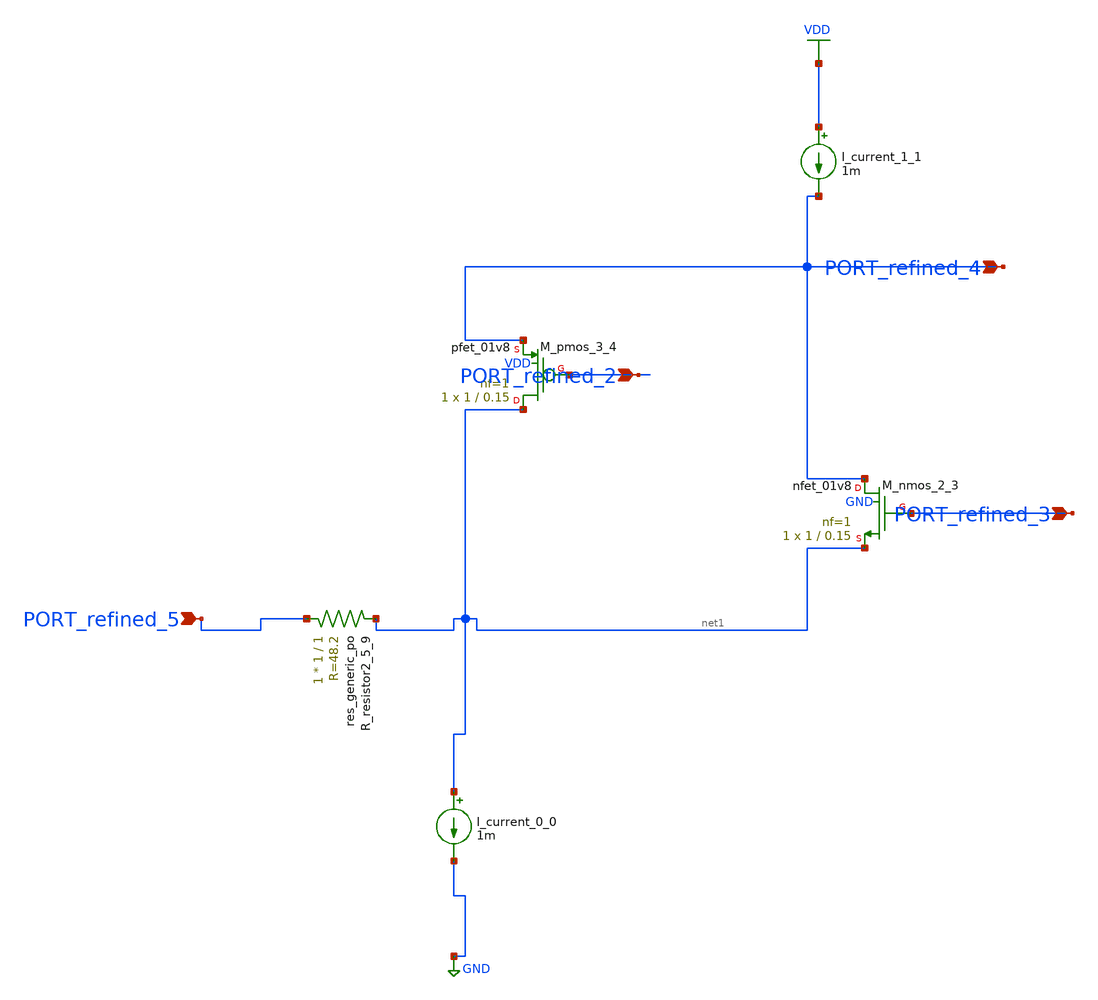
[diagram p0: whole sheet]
** sch_path: schematics/AMSNet/415.sch
**.subckt 415 PORT_refined_3 PORT_refined_4 PORT_refined_5 PORT_refined_2
*.ipin PORT_refined_3
*.ipin PORT_refined_4
*.ipin PORT_refined_5
*.ipin PORT_refined_2
I_current_0_0 net1 GND 1m
I_current_1_1 VDD PORT_refined_4 1m
XM_nmos_2_3 PORT_refined_4 PORT_refined_3 net1 GND sky130_fd_pr__nfet_01v8 L=0.15 W=1 nf=1 ad='int((1 + 1)/2) * 1 / 1 * 0.29'
+ as='int((1 + 2)/2) * 1 / 1 * 0.29' pd='2*int((1 + 1)/2) * (1 / 1 + 0.29)' ps='2*int((1 + 2)/2) * (1 / 1 + 0.29)'
+ nrd='0.29 / 1 ' nrs='0.29 / 1 ' sa=0 sb=0 sd=0 mult=1 m=1
XM_pmos_3_4 net1 PORT_refined_2 PORT_refined_4 VDD sky130_fd_pr__pfet_01v8 L=0.15 W=1 nf=1 ad='int((1 + 1)/2) * 1 / 1 * 0.29'
+ as='int((1 + 2)/2) * 1 / 1 * 0.29' pd='2*int((1 + 1)/2) * (1 / 1 + 0.29)' ps='2*int((1 + 2)/2) * (1 / 1 + 0.29)'
+ nrd='0.29 / 1 ' nrs='0.29 / 1 ' sa=0 sb=0 sd=0 mult=1 m=1
XR_resistor2_5_9 PORT_refined_5 net1 sky130_fd_pr__res_generic_po W=1 L=1 m=1
**.ends
.GLOBAL GND
.GLOBAL VDD
.end
